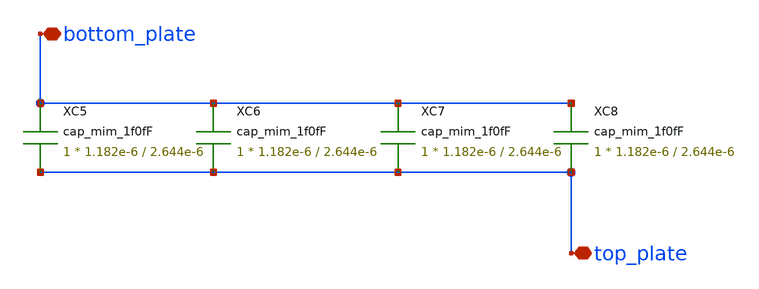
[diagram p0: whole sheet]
** sch_path: CDAC/4C.sch
**.subckt 4C top_plate bottom_plate
*.iopin top_plate
*.iopin bottom_plate
XC5 bottom_plate top_plate cap_mim_1f0fF c_width=1.182e-6 c_length=2.644e-6 m=1
XC6 bottom_plate top_plate cap_mim_1f0fF c_width=1.182e-6 c_length=2.644e-6 m=1
XC7 bottom_plate top_plate cap_mim_1f0fF c_width=1.182e-6 c_length=2.644e-6 m=1
XC8 bottom_plate top_plate cap_mim_1f0fF c_width=1.182e-6 c_length=2.644e-6 m=1
**.ends
.end
